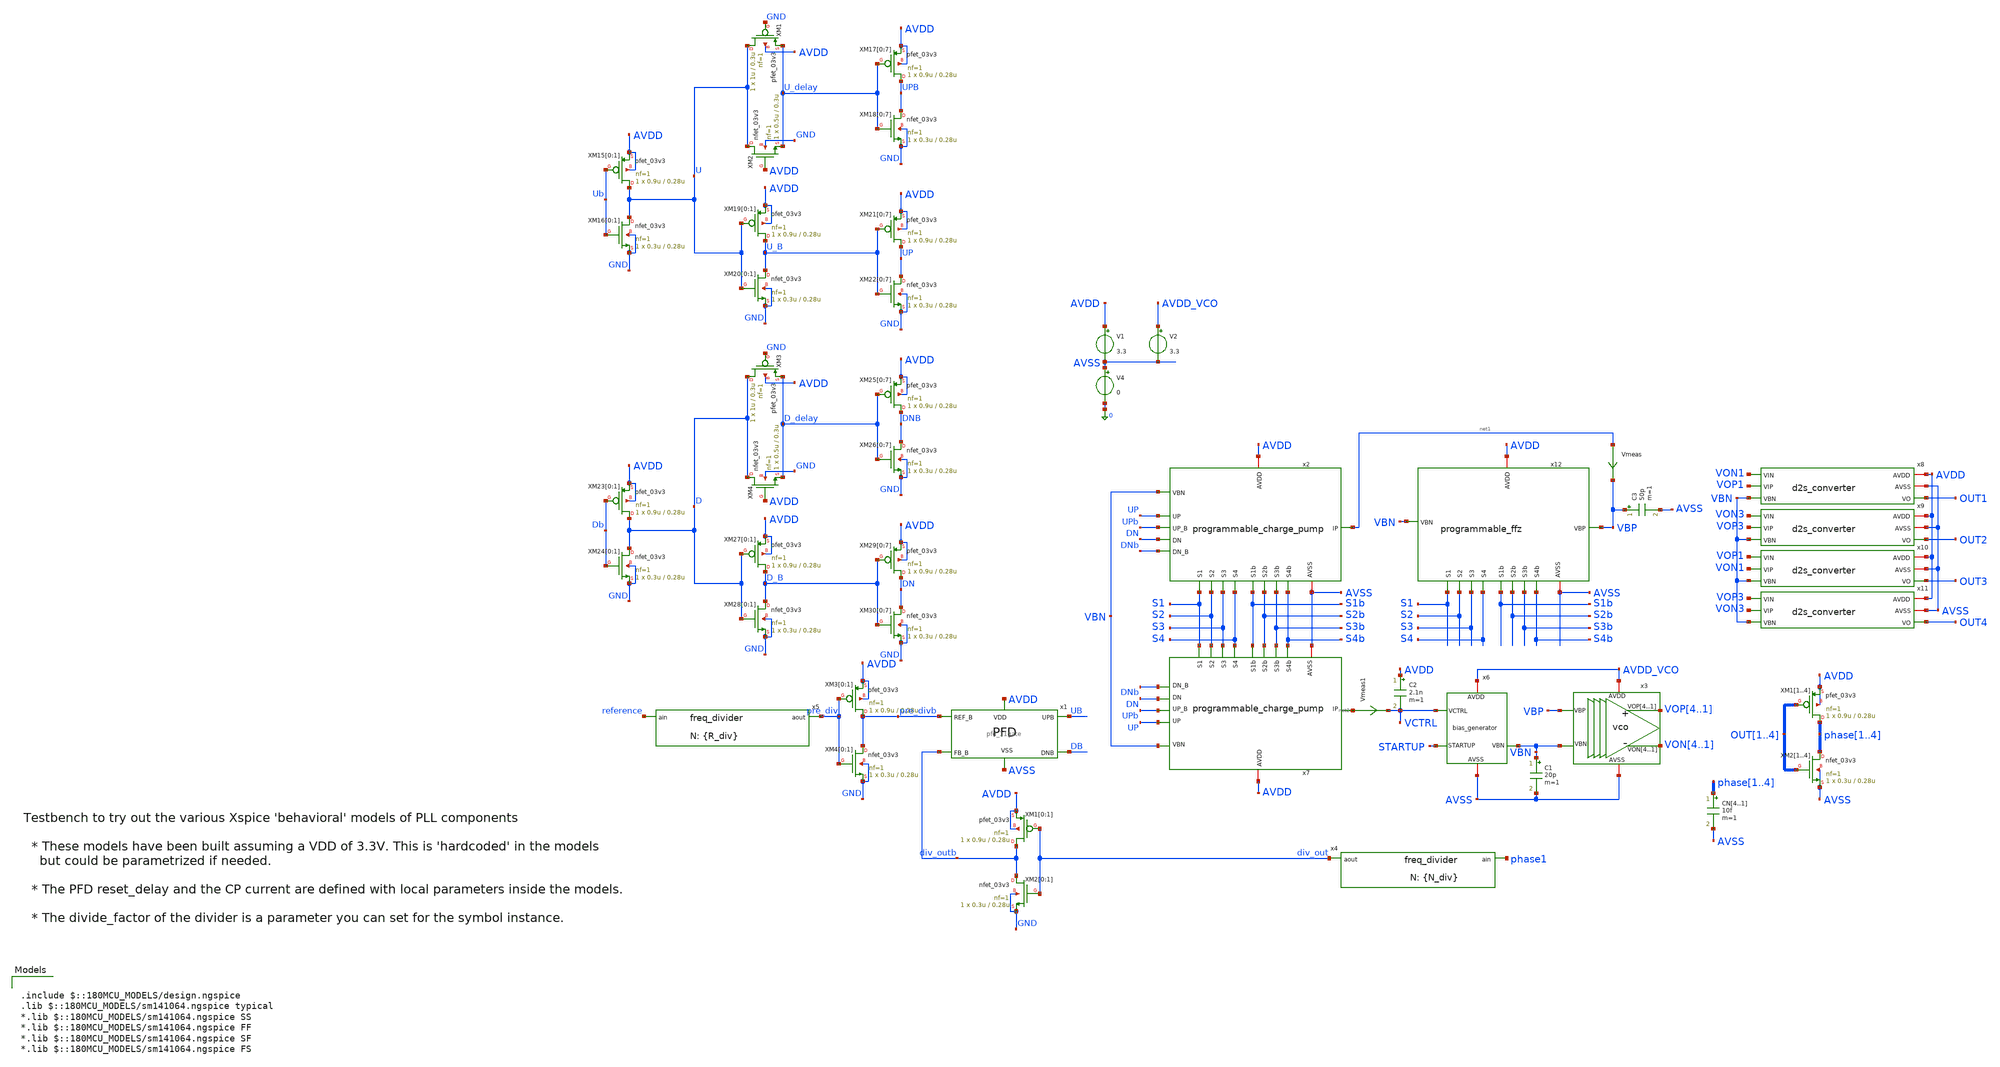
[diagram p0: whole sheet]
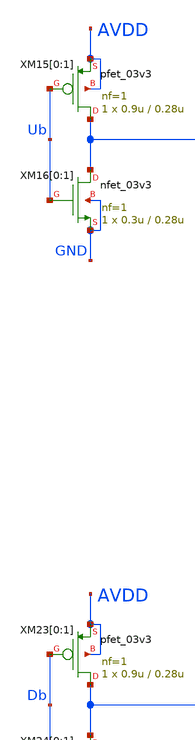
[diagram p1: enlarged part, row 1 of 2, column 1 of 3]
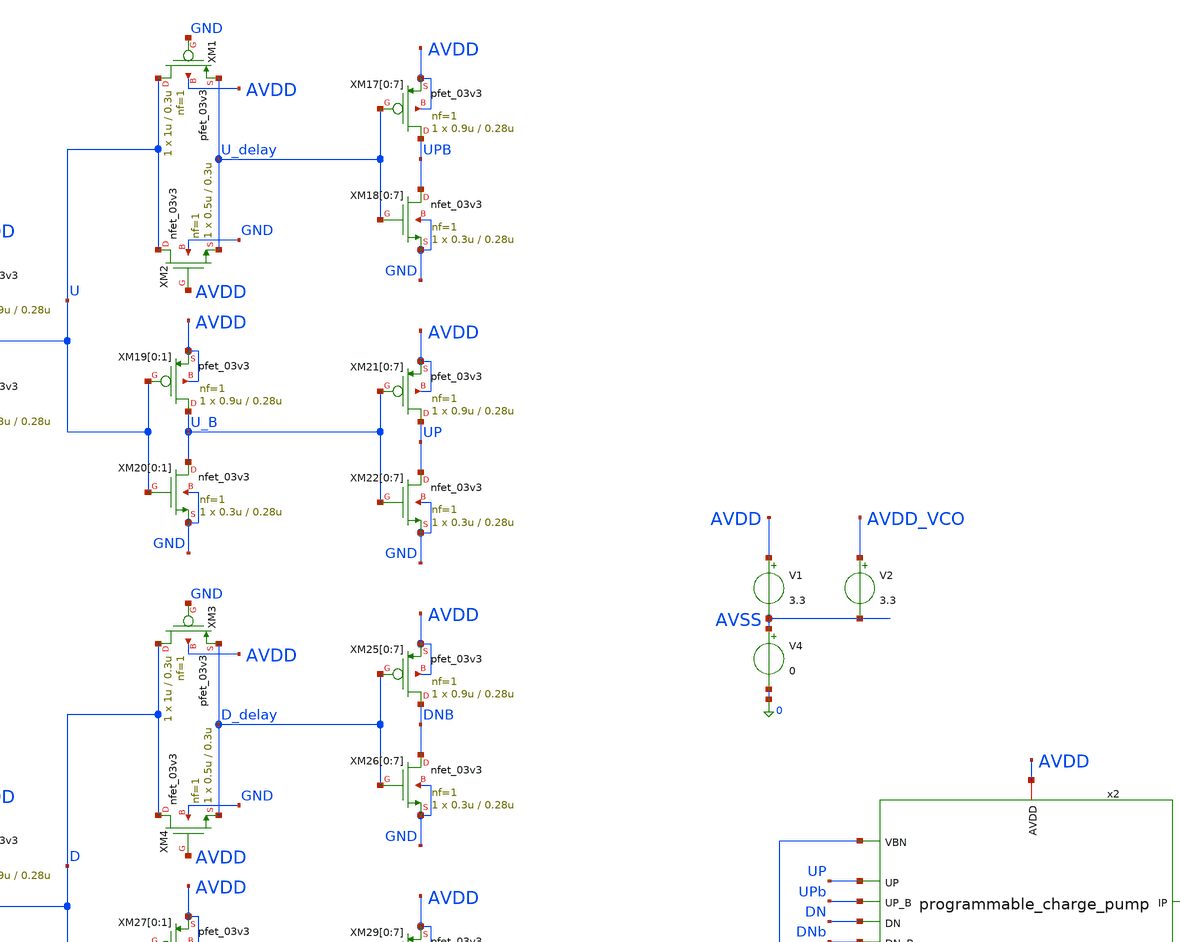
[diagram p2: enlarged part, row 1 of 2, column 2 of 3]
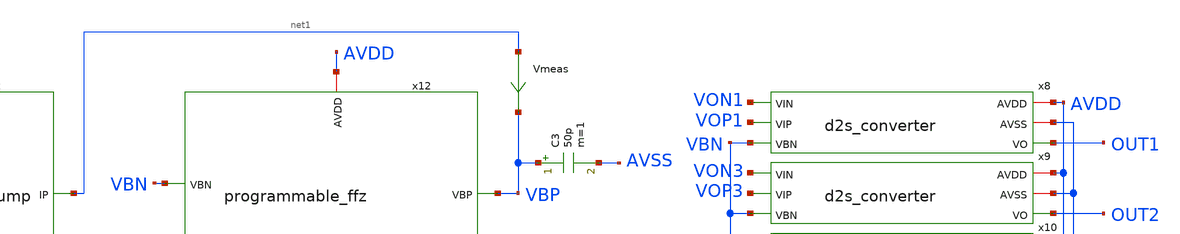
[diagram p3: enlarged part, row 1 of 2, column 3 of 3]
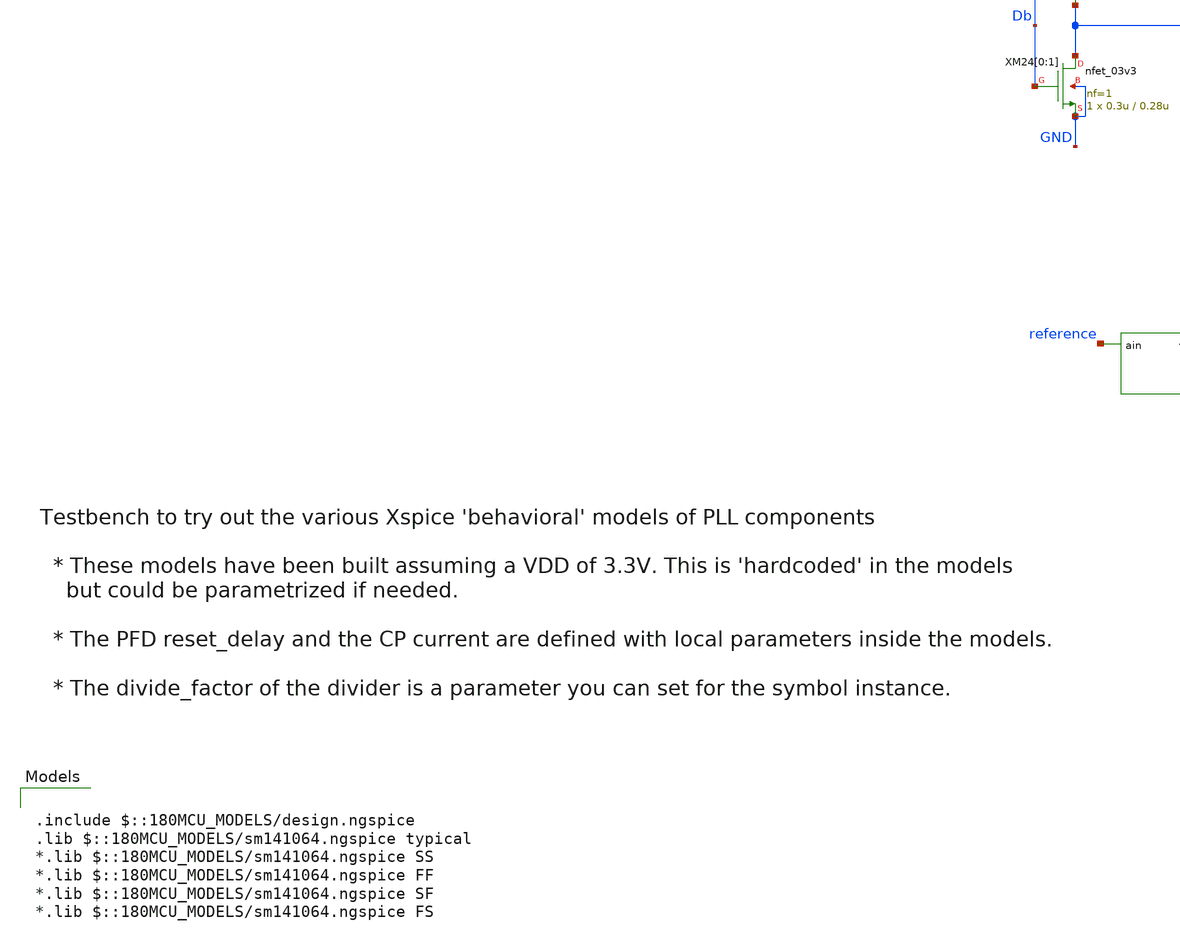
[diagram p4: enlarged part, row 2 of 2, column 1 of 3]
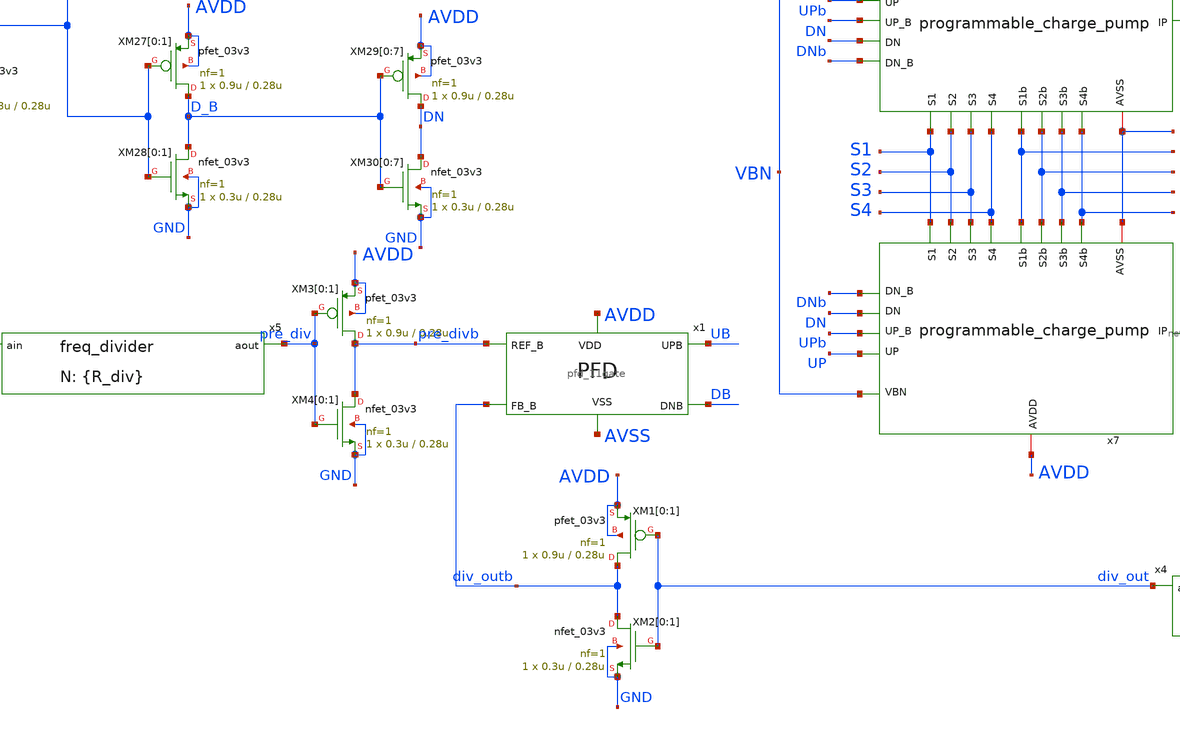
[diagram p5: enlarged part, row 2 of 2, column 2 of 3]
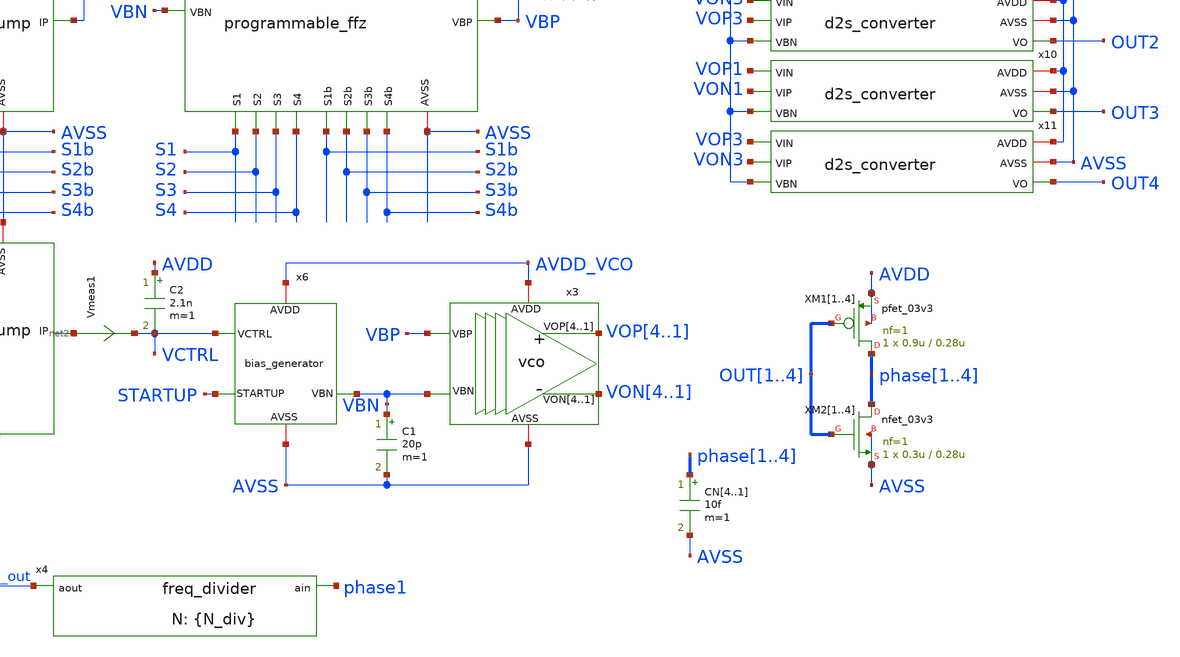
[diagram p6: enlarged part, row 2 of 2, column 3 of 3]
** sch_path: designs/libs/tb_pll/tb_PLL_CP_VCO_PFD_model.sch
**.subckt tb_PLL_CP_VCO_PFD_model
x4 div_out phase1 freq_divider divide_factor={N_div}
x5 pre_div reference freq_divider divide_factor={R_div}
x3 VOP4 VOP3 VOP2 VOP1 VON4 VON3 VON2 VON1 AVDD_VCO AVSS VBP VBN vco
x6 VCTRL AVDD_VCO STARTUP AVSS VBN bias_generator
C2 AVDD VCTRL 2.1n m=1
x8 AVDD AVSS VON1 VOP1 VBN OUT1 d2s_converter
XM11 phase1 OUT1 AVDD AVDD pfet_03v3 L=0.28u W=0.9u nf=1 ad='int((nf+1)/2) * W/nf * 0.18u' as='int((nf+2)/2) * W/nf * 0.18u'
+ pd='2*int((nf+1)/2) * (W/nf + 0.18u)' ps='2*int((nf+2)/2) * (W/nf + 0.18u)' nrd='0.18u / W' nrs='0.18u / W'
+ sa=0 sb=0 sd=0 m=1
XM12 phase2 OUT2 AVDD AVDD pfet_03v3 L=0.28u W=0.9u nf=1 ad='int((nf+1)/2) * W/nf * 0.18u' as='int((nf+2)/2) * W/nf * 0.18u'
+ pd='2*int((nf+1)/2) * (W/nf + 0.18u)' ps='2*int((nf+2)/2) * (W/nf + 0.18u)' nrd='0.18u / W' nrs='0.18u / W'
+ sa=0 sb=0 sd=0 m=1
XM13 phase3 OUT3 AVDD AVDD pfet_03v3 L=0.28u W=0.9u nf=1 ad='int((nf+1)/2) * W/nf * 0.18u' as='int((nf+2)/2) * W/nf * 0.18u'
+ pd='2*int((nf+1)/2) * (W/nf + 0.18u)' ps='2*int((nf+2)/2) * (W/nf + 0.18u)' nrd='0.18u / W' nrs='0.18u / W'
+ sa=0 sb=0 sd=0 m=1
XM14 phase4 OUT4 AVDD AVDD pfet_03v3 L=0.28u W=0.9u nf=1 ad='int((nf+1)/2) * W/nf * 0.18u' as='int((nf+2)/2) * W/nf * 0.18u'
+ pd='2*int((nf+1)/2) * (W/nf + 0.18u)' ps='2*int((nf+2)/2) * (W/nf + 0.18u)' nrd='0.18u / W' nrs='0.18u / W'
+ sa=0 sb=0 sd=0 m=1
XM21 phase1 OUT1 AVSS AVSS nfet_03v3 L=0.28u W=0.3u nf=1 ad='int((nf+1)/2) * W/nf * 0.18u' as='int((nf+2)/2) * W/nf * 0.18u'
+ pd='2*int((nf+1)/2) * (W/nf + 0.18u)' ps='2*int((nf+2)/2) * (W/nf + 0.18u)' nrd='0.18u / W' nrs='0.18u / W'
+ sa=0 sb=0 sd=0 m=1
XM22 phase2 OUT2 AVSS AVSS nfet_03v3 L=0.28u W=0.3u nf=1 ad='int((nf+1)/2) * W/nf * 0.18u' as='int((nf+2)/2) * W/nf * 0.18u'
+ pd='2*int((nf+1)/2) * (W/nf + 0.18u)' ps='2*int((nf+2)/2) * (W/nf + 0.18u)' nrd='0.18u / W' nrs='0.18u / W'
+ sa=0 sb=0 sd=0 m=1
XM23 phase3 OUT3 AVSS AVSS nfet_03v3 L=0.28u W=0.3u nf=1 ad='int((nf+1)/2) * W/nf * 0.18u' as='int((nf+2)/2) * W/nf * 0.18u'
+ pd='2*int((nf+1)/2) * (W/nf + 0.18u)' ps='2*int((nf+2)/2) * (W/nf + 0.18u)' nrd='0.18u / W' nrs='0.18u / W'
+ sa=0 sb=0 sd=0 m=1
XM24 phase4 OUT4 AVSS AVSS nfet_03v3 L=0.28u W=0.3u nf=1 ad='int((nf+1)/2) * W/nf * 0.18u' as='int((nf+2)/2) * W/nf * 0.18u'
+ pd='2*int((nf+1)/2) * (W/nf + 0.18u)' ps='2*int((nf+2)/2) * (W/nf + 0.18u)' nrd='0.18u / W' nrs='0.18u / W'
+ sa=0 sb=0 sd=0 m=1
x9 AVDD AVSS VON3 VOP3 VBN OUT2 d2s_converter
x10 AVDD AVSS VOP1 VON1 VBN OUT3 d2s_converter
x11 AVDD AVSS VOP3 VON3 VBN OUT4 d2s_converter
V1 AVDD AVSS 3.3
V4 AVSS 0 0
V2 AVDD_VCO AVSS 3.3
x2 AVSS AVDD UP UPb DN net1 DNb VBN S1b S1 S2b S2 S3b S3 S4b S4 programmable_charge_pump
x7 AVSS AVDD UP UPb DN net2 DNb VBN S1b S1 S2b S2 S3b S3 S4b S4 programmable_charge_pump
CN4 phase1 AVSS 10f m=1
CN3 phase2 AVSS 10f m=1
CN2 phase3 AVSS 10f m=1
CN1 phase4 AVSS 10f m=1
Vmeas net1 VBP 0
.save i(vmeas)
Vmeas1 net2 VCTRL 0
.save i(vmeas1)
C1 VBN AVSS 20p m=1
C3 VBP AVSS 50p m=1
x12 VBP AVSS AVDD VBN S1b S1 S2b S2 S3b S3 S4b S4 programmable_ffz
x1 pre_divb UB DB div_outb AVDD AVSS pfd_11gate
XM15[0] U Ub AVDD AVDD pfet_03v3 L=0.28u W=0.9u nf=1 ad='int((nf+1)/2) * W/nf * 0.18u' as='int((nf+2)/2) * W/nf * 0.18u'
+ pd='2*int((nf+1)/2) * (W/nf + 0.18u)' ps='2*int((nf+2)/2) * (W/nf + 0.18u)' nrd='0.18u / W' nrs='0.18u / W'
+ sa=0 sb=0 sd=0 m=1
XM15[1] U Ub AVDD AVDD pfet_03v3 L=0.28u W=0.9u nf=1 ad='int((nf+1)/2) * W/nf * 0.18u' as='int((nf+2)/2) * W/nf * 0.18u'
+ pd='2*int((nf+1)/2) * (W/nf + 0.18u)' ps='2*int((nf+2)/2) * (W/nf + 0.18u)' nrd='0.18u / W' nrs='0.18u / W'
+ sa=0 sb=0 sd=0 m=1
XM16[0] U Ub GND GND nfet_03v3 L=0.28u W=0.3u nf=1 ad='int((nf+1)/2) * W/nf * 0.18u' as='int((nf+2)/2) * W/nf * 0.18u'
+ pd='2*int((nf+1)/2) * (W/nf + 0.18u)' ps='2*int((nf+2)/2) * (W/nf + 0.18u)' nrd='0.18u / W' nrs='0.18u / W'
+ sa=0 sb=0 sd=0 m=1
XM16[1] U Ub GND GND nfet_03v3 L=0.28u W=0.3u nf=1 ad='int((nf+1)/2) * W/nf * 0.18u' as='int((nf+2)/2) * W/nf * 0.18u'
+ pd='2*int((nf+1)/2) * (W/nf + 0.18u)' ps='2*int((nf+2)/2) * (W/nf + 0.18u)' nrd='0.18u / W' nrs='0.18u / W'
+ sa=0 sb=0 sd=0 m=1
XM1 U GND U_delay AVDD pfet_03v3 L=0.3u W=1u nf=1 ad='int((nf+1)/2) * W/nf * 0.18u' as='int((nf+2)/2) * W/nf * 0.18u'
+ pd='2*int((nf+1)/2) * (W/nf + 0.18u)' ps='2*int((nf+2)/2) * (W/nf + 0.18u)' nrd='0.18u / W' nrs='0.18u / W'
+ sa=0 sb=0 sd=0 m=1
XM2 U AVDD U_delay GND nfet_03v3 L=0.3u W=0.5u nf=1 ad='int((nf+1)/2) * W/nf * 0.18u' as='int((nf+2)/2) * W/nf * 0.18u'
+ pd='2*int((nf+1)/2) * (W/nf + 0.18u)' ps='2*int((nf+2)/2) * (W/nf + 0.18u)' nrd='0.18u / W' nrs='0.18u / W'
+ sa=0 sb=0 sd=0 m=1
XM17[0] UPB U_delay AVDD AVDD pfet_03v3 L=0.28u W=0.9u nf=1 ad='int((nf+1)/2) * W/nf * 0.18u' as='int((nf+2)/2) * W/nf * 0.18u'
+ pd='2*int((nf+1)/2) * (W/nf + 0.18u)' ps='2*int((nf+2)/2) * (W/nf + 0.18u)' nrd='0.18u / W' nrs='0.18u / W'
+ sa=0 sb=0 sd=0 m=1
XM17[1] UPB U_delay AVDD AVDD pfet_03v3 L=0.28u W=0.9u nf=1 ad='int((nf+1)/2) * W/nf * 0.18u' as='int((nf+2)/2) * W/nf * 0.18u'
+ pd='2*int((nf+1)/2) * (W/nf + 0.18u)' ps='2*int((nf+2)/2) * (W/nf + 0.18u)' nrd='0.18u / W' nrs='0.18u / W'
+ sa=0 sb=0 sd=0 m=1
XM17[2] UPB U_delay AVDD AVDD pfet_03v3 L=0.28u W=0.9u nf=1 ad='int((nf+1)/2) * W/nf * 0.18u' as='int((nf+2)/2) * W/nf * 0.18u'
+ pd='2*int((nf+1)/2) * (W/nf + 0.18u)' ps='2*int((nf+2)/2) * (W/nf + 0.18u)' nrd='0.18u / W' nrs='0.18u / W'
+ sa=0 sb=0 sd=0 m=1
XM17[3] UPB U_delay AVDD AVDD pfet_03v3 L=0.28u W=0.9u nf=1 ad='int((nf+1)/2) * W/nf * 0.18u' as='int((nf+2)/2) * W/nf * 0.18u'
+ pd='2*int((nf+1)/2) * (W/nf + 0.18u)' ps='2*int((nf+2)/2) * (W/nf + 0.18u)' nrd='0.18u / W' nrs='0.18u / W'
+ sa=0 sb=0 sd=0 m=1
XM17[4] UPB U_delay AVDD AVDD pfet_03v3 L=0.28u W=0.9u nf=1 ad='int((nf+1)/2) * W/nf * 0.18u' as='int((nf+2)/2) * W/nf * 0.18u'
+ pd='2*int((nf+1)/2) * (W/nf + 0.18u)' ps='2*int((nf+2)/2) * (W/nf + 0.18u)' nrd='0.18u / W' nrs='0.18u / W'
+ sa=0 sb=0 sd=0 m=1
XM17[5] UPB U_delay AVDD AVDD pfet_03v3 L=0.28u W=0.9u nf=1 ad='int((nf+1)/2) * W/nf * 0.18u' as='int((nf+2)/2) * W/nf * 0.18u'
+ pd='2*int((nf+1)/2) * (W/nf + 0.18u)' ps='2*int((nf+2)/2) * (W/nf + 0.18u)' nrd='0.18u / W' nrs='0.18u / W'
+ sa=0 sb=0 sd=0 m=1
XM17[6] UPB U_delay AVDD AVDD pfet_03v3 L=0.28u W=0.9u nf=1 ad='int((nf+1)/2) * W/nf * 0.18u' as='int((nf+2)/2) * W/nf * 0.18u'
+ pd='2*int((nf+1)/2) * (W/nf + 0.18u)' ps='2*int((nf+2)/2) * (W/nf + 0.18u)' nrd='0.18u / W' nrs='0.18u / W'
+ sa=0 sb=0 sd=0 m=1
XM17[7] UPB U_delay AVDD AVDD pfet_03v3 L=0.28u W=0.9u nf=1 ad='int((nf+1)/2) * W/nf * 0.18u' as='int((nf+2)/2) * W/nf * 0.18u'
+ pd='2*int((nf+1)/2) * (W/nf + 0.18u)' ps='2*int((nf+2)/2) * (W/nf + 0.18u)' nrd='0.18u / W' nrs='0.18u / W'
+ sa=0 sb=0 sd=0 m=1
XM18[0] UPB U_delay GND GND nfet_03v3 L=0.28u W=0.3u nf=1 ad='int((nf+1)/2) * W/nf * 0.18u' as='int((nf+2)/2) * W/nf * 0.18u'
+ pd='2*int((nf+1)/2) * (W/nf + 0.18u)' ps='2*int((nf+2)/2) * (W/nf + 0.18u)' nrd='0.18u / W' nrs='0.18u / W'
+ sa=0 sb=0 sd=0 m=1
XM18[1] UPB U_delay GND GND nfet_03v3 L=0.28u W=0.3u nf=1 ad='int((nf+1)/2) * W/nf * 0.18u' as='int((nf+2)/2) * W/nf * 0.18u'
+ pd='2*int((nf+1)/2) * (W/nf + 0.18u)' ps='2*int((nf+2)/2) * (W/nf + 0.18u)' nrd='0.18u / W' nrs='0.18u / W'
+ sa=0 sb=0 sd=0 m=1
XM18[2] UPB U_delay GND GND nfet_03v3 L=0.28u W=0.3u nf=1 ad='int((nf+1)/2) * W/nf * 0.18u' as='int((nf+2)/2) * W/nf * 0.18u'
+ pd='2*int((nf+1)/2) * (W/nf + 0.18u)' ps='2*int((nf+2)/2) * (W/nf + 0.18u)' nrd='0.18u / W' nrs='0.18u / W'
+ sa=0 sb=0 sd=0 m=1
XM18[3] UPB U_delay GND GND nfet_03v3 L=0.28u W=0.3u nf=1 ad='int((nf+1)/2) * W/nf * 0.18u' as='int((nf+2)/2) * W/nf * 0.18u'
+ pd='2*int((nf+1)/2) * (W/nf + 0.18u)' ps='2*int((nf+2)/2) * (W/nf + 0.18u)' nrd='0.18u / W' nrs='0.18u / W'
+ sa=0 sb=0 sd=0 m=1
XM18[4] UPB U_delay GND GND nfet_03v3 L=0.28u W=0.3u nf=1 ad='int((nf+1)/2) * W/nf * 0.18u' as='int((nf+2)/2) * W/nf * 0.18u'
+ pd='2*int((nf+1)/2) * (W/nf + 0.18u)' ps='2*int((nf+2)/2) * (W/nf + 0.18u)' nrd='0.18u / W' nrs='0.18u / W'
+ sa=0 sb=0 sd=0 m=1
XM18[5] UPB U_delay GND GND nfet_03v3 L=0.28u W=0.3u nf=1 ad='int((nf+1)/2) * W/nf * 0.18u' as='int((nf+2)/2) * W/nf * 0.18u'
+ pd='2*int((nf+1)/2) * (W/nf + 0.18u)' ps='2*int((nf+2)/2) * (W/nf + 0.18u)' nrd='0.18u / W' nrs='0.18u / W'
+ sa=0 sb=0 sd=0 m=1
XM18[6] UPB U_delay GND GND nfet_03v3 L=0.28u W=0.3u nf=1 ad='int((nf+1)/2) * W/nf * 0.18u' as='int((nf+2)/2) * W/nf * 0.18u'
+ pd='2*int((nf+1)/2) * (W/nf + 0.18u)' ps='2*int((nf+2)/2) * (W/nf + 0.18u)' nrd='0.18u / W' nrs='0.18u / W'
+ sa=0 sb=0 sd=0 m=1
XM18[7] UPB U_delay GND GND nfet_03v3 L=0.28u W=0.3u nf=1 ad='int((nf+1)/2) * W/nf * 0.18u' as='int((nf+2)/2) * W/nf * 0.18u'
+ pd='2*int((nf+1)/2) * (W/nf + 0.18u)' ps='2*int((nf+2)/2) * (W/nf + 0.18u)' nrd='0.18u / W' nrs='0.18u / W'
+ sa=0 sb=0 sd=0 m=1
XM19[0] U_B U AVDD AVDD pfet_03v3 L=0.28u W=0.9u nf=1 ad='int((nf+1)/2) * W/nf * 0.18u' as='int((nf+2)/2) * W/nf * 0.18u'
+ pd='2*int((nf+1)/2) * (W/nf + 0.18u)' ps='2*int((nf+2)/2) * (W/nf + 0.18u)' nrd='0.18u / W' nrs='0.18u / W'
+ sa=0 sb=0 sd=0 m=1
XM19[1] U_B U AVDD AVDD pfet_03v3 L=0.28u W=0.9u nf=1 ad='int((nf+1)/2) * W/nf * 0.18u' as='int((nf+2)/2) * W/nf * 0.18u'
+ pd='2*int((nf+1)/2) * (W/nf + 0.18u)' ps='2*int((nf+2)/2) * (W/nf + 0.18u)' nrd='0.18u / W' nrs='0.18u / W'
+ sa=0 sb=0 sd=0 m=1
XM20[0] U_B U GND GND nfet_03v3 L=0.28u W=0.3u nf=1 ad='int((nf+1)/2) * W/nf * 0.18u' as='int((nf+2)/2) * W/nf * 0.18u'
+ pd='2*int((nf+1)/2) * (W/nf + 0.18u)' ps='2*int((nf+2)/2) * (W/nf + 0.18u)' nrd='0.18u / W' nrs='0.18u / W'
+ sa=0 sb=0 sd=0 m=1
XM20[1] U_B U GND GND nfet_03v3 L=0.28u W=0.3u nf=1 ad='int((nf+1)/2) * W/nf * 0.18u' as='int((nf+2)/2) * W/nf * 0.18u'
+ pd='2*int((nf+1)/2) * (W/nf + 0.18u)' ps='2*int((nf+2)/2) * (W/nf + 0.18u)' nrd='0.18u / W' nrs='0.18u / W'
+ sa=0 sb=0 sd=0 m=1
XM21[0] UP U_B AVDD AVDD pfet_03v3 L=0.28u W=0.9u nf=1 ad='int((nf+1)/2) * W/nf * 0.18u' as='int((nf+2)/2) * W/nf * 0.18u'
+ pd='2*int((nf+1)/2) * (W/nf + 0.18u)' ps='2*int((nf+2)/2) * (W/nf + 0.18u)' nrd='0.18u / W' nrs='0.18u / W'
+ sa=0 sb=0 sd=0 m=1
XM21[1] UP U_B AVDD AVDD pfet_03v3 L=0.28u W=0.9u nf=1 ad='int((nf+1)/2) * W/nf * 0.18u' as='int((nf+2)/2) * W/nf * 0.18u'
+ pd='2*int((nf+1)/2) * (W/nf + 0.18u)' ps='2*int((nf+2)/2) * (W/nf + 0.18u)' nrd='0.18u / W' nrs='0.18u / W'
+ sa=0 sb=0 sd=0 m=1
XM21[2] UP U_B AVDD AVDD pfet_03v3 L=0.28u W=0.9u nf=1 ad='int((nf+1)/2) * W/nf * 0.18u' as='int((nf+2)/2) * W/nf * 0.18u'
+ pd='2*int((nf+1)/2) * (W/nf + 0.18u)' ps='2*int((nf+2)/2) * (W/nf + 0.18u)' nrd='0.18u / W' nrs='0.18u / W'
+ sa=0 sb=0 sd=0 m=1
XM21[3] UP U_B AVDD AVDD pfet_03v3 L=0.28u W=0.9u nf=1 ad='int((nf+1)/2) * W/nf * 0.18u' as='int((nf+2)/2) * W/nf * 0.18u'
+ pd='2*int((nf+1)/2) * (W/nf + 0.18u)' ps='2*int((nf+2)/2) * (W/nf + 0.18u)' nrd='0.18u / W' nrs='0.18u / W'
+ sa=0 sb=0 sd=0 m=1
XM21[4] UP U_B AVDD AVDD pfet_03v3 L=0.28u W=0.9u nf=1 ad='int((nf+1)/2) * W/nf * 0.18u' as='int((nf+2)/2) * W/nf * 0.18u'
+ pd='2*int((nf+1)/2) * (W/nf + 0.18u)' ps='2*int((nf+2)/2) * (W/nf + 0.18u)' nrd='0.18u / W' nrs='0.18u / W'
+ sa=0 sb=0 sd=0 m=1
XM21[5] UP U_B AVDD AVDD pfet_03v3 L=0.28u W=0.9u nf=1 ad='int((nf+1)/2) * W/nf * 0.18u' as='int((nf+2)/2) * W/nf * 0.18u'
+ pd='2*int((nf+1)/2) * (W/nf + 0.18u)' ps='2*int((nf+2)/2) * (W/nf + 0.18u)' nrd='0.18u / W' nrs='0.18u / W'
+ sa=0 sb=0 sd=0 m=1
XM21[6] UP U_B AVDD AVDD pfet_03v3 L=0.28u W=0.9u nf=1 ad='int((nf+1)/2) * W/nf * 0.18u' as='int((nf+2)/2) * W/nf * 0.18u'
+ pd='2*int((nf+1)/2) * (W/nf + 0.18u)' ps='2*int((nf+2)/2) * (W/nf + 0.18u)' nrd='0.18u / W' nrs='0.18u / W'
+ sa=0 sb=0 sd=0 m=1
XM21[7] UP U_B AVDD AVDD pfet_03v3 L=0.28u W=0.9u nf=1 ad='int((nf+1)/2) * W/nf * 0.18u' as='int((nf+2)/2) * W/nf * 0.18u'
+ pd='2*int((nf+1)/2) * (W/nf + 0.18u)' ps='2*int((nf+2)/2) * (W/nf + 0.18u)' nrd='0.18u / W' nrs='0.18u / W'
+ sa=0 sb=0 sd=0 m=1
XM22[0] UP U_B GND GND nfet_03v3 L=0.28u W=0.3u nf=1 ad='int((nf+1)/2) * W/nf * 0.18u' as='int((nf+2)/2) * W/nf * 0.18u'
+ pd='2*int((nf+1)/2) * (W/nf + 0.18u)' ps='2*int((nf+2)/2) * (W/nf + 0.18u)' nrd='0.18u / W' nrs='0.18u / W'
+ sa=0 sb=0 sd=0 m=1
XM22[1] UP U_B GND GND nfet_03v3 L=0.28u W=0.3u nf=1 ad='int((nf+1)/2) * W/nf * 0.18u' as='int((nf+2)/2) * W/nf * 0.18u'
+ pd='2*int((nf+1)/2) * (W/nf + 0.18u)' ps='2*int((nf+2)/2) * (W/nf + 0.18u)' nrd='0.18u / W' nrs='0.18u / W'
+ sa=0 sb=0 sd=0 m=1
XM22[2] UP U_B GND GND nfet_03v3 L=0.28u W=0.3u nf=1 ad='int((nf+1)/2) * W/nf * 0.18u' as='int((nf+2)/2) * W/nf * 0.18u'
+ pd='2*int((nf+1)/2) * (W/nf + 0.18u)' ps='2*int((nf+2)/2) * (W/nf + 0.18u)' nrd='0.18u / W' nrs='0.18u / W'
+ sa=0 sb=0 sd=0 m=1
XM22[3] UP U_B GND GND nfet_03v3 L=0.28u W=0.3u nf=1 ad='int((nf+1)/2) * W/nf * 0.18u' as='int((nf+2)/2) * W/nf * 0.18u'
+ pd='2*int((nf+1)/2) * (W/nf + 0.18u)' ps='2*int((nf+2)/2) * (W/nf + 0.18u)' nrd='0.18u / W' nrs='0.18u / W'
+ sa=0 sb=0 sd=0 m=1
XM22[4] UP U_B GND GND nfet_03v3 L=0.28u W=0.3u nf=1 ad='int((nf+1)/2) * W/nf * 0.18u' as='int((nf+2)/2) * W/nf * 0.18u'
+ pd='2*int((nf+1)/2) * (W/nf + 0.18u)' ps='2*int((nf+2)/2) * (W/nf + 0.18u)' nrd='0.18u / W' nrs='0.18u / W'
+ sa=0 sb=0 sd=0 m=1
XM22[5] UP U_B GND GND nfet_03v3 L=0.28u W=0.3u nf=1 ad='int((nf+1)/2) * W/nf * 0.18u' as='int((nf+2)/2) * W/nf * 0.18u'
+ pd='2*int((nf+1)/2) * (W/nf + 0.18u)' ps='2*int((nf+2)/2) * (W/nf + 0.18u)' nrd='0.18u / W' nrs='0.18u / W'
+ sa=0 sb=0 sd=0 m=1
XM22[6] UP U_B GND GND nfet_03v3 L=0.28u W=0.3u nf=1 ad='int((nf+1)/2) * W/nf * 0.18u' as='int((nf+2)/2) * W/nf * 0.18u'
+ pd='2*int((nf+1)/2) * (W/nf + 0.18u)' ps='2*int((nf+2)/2) * (W/nf + 0.18u)' nrd='0.18u / W' nrs='0.18u / W'
+ sa=0 sb=0 sd=0 m=1
XM22[7] UP U_B GND GND nfet_03v3 L=0.28u W=0.3u nf=1 ad='int((nf+1)/2) * W/nf * 0.18u' as='int((nf+2)/2) * W/nf * 0.18u'
+ pd='2*int((nf+1)/2) * (W/nf + 0.18u)' ps='2*int((nf+2)/2) * (W/nf + 0.18u)' nrd='0.18u / W' nrs='0.18u / W'
+ sa=0 sb=0 sd=0 m=1
XM23[0] D Db AVDD AVDD pfet_03v3 L=0.28u W=0.9u nf=1 ad='int((nf+1)/2) * W/nf * 0.18u' as='int((nf+2)/2) * W/nf * 0.18u'
+ pd='2*int((nf+1)/2) * (W/nf + 0.18u)' ps='2*int((nf+2)/2) * (W/nf + 0.18u)' nrd='0.18u / W' nrs='0.18u / W'
+ sa=0 sb=0 sd=0 m=1
XM23[1] D Db AVDD AVDD pfet_03v3 L=0.28u W=0.9u nf=1 ad='int((nf+1)/2) * W/nf * 0.18u' as='int((nf+2)/2) * W/nf * 0.18u'
+ pd='2*int((nf+1)/2) * (W/nf + 0.18u)' ps='2*int((nf+2)/2) * (W/nf + 0.18u)' nrd='0.18u / W' nrs='0.18u / W'
+ sa=0 sb=0 sd=0 m=1
XM24[0] D Db GND GND nfet_03v3 L=0.28u W=0.3u nf=1 ad='int((nf+1)/2) * W/nf * 0.18u' as='int((nf+2)/2) * W/nf * 0.18u'
+ pd='2*int((nf+1)/2) * (W/nf + 0.18u)' ps='2*int((nf+2)/2) * (W/nf + 0.18u)' nrd='0.18u / W' nrs='0.18u / W'
+ sa=0 sb=0 sd=0 m=1
XM24[1] D Db GND GND nfet_03v3 L=0.28u W=0.3u nf=1 ad='int((nf+1)/2) * W/nf * 0.18u' as='int((nf+2)/2) * W/nf * 0.18u'
+ pd='2*int((nf+1)/2) * (W/nf + 0.18u)' ps='2*int((nf+2)/2) * (W/nf + 0.18u)' nrd='0.18u / W' nrs='0.18u / W'
+ sa=0 sb=0 sd=0 m=1
XM25[0] DNB D_delay AVDD AVDD pfet_03v3 L=0.28u W=0.9u nf=1 ad='int((nf+1)/2) * W/nf * 0.18u' as='int((nf+2)/2) * W/nf * 0.18u'
+ pd='2*int((nf+1)/2) * (W/nf + 0.18u)' ps='2*int((nf+2)/2) * (W/nf + 0.18u)' nrd='0.18u / W' nrs='0.18u / W'
+ sa=0 sb=0 sd=0 m=1
XM25[1] DNB D_delay AVDD AVDD pfet_03v3 L=0.28u W=0.9u nf=1 ad='int((nf+1)/2) * W/nf * 0.18u' as='int((nf+2)/2) * W/nf * 0.18u'
+ pd='2*int((nf+1)/2) * (W/nf + 0.18u)' ps='2*int((nf+2)/2) * (W/nf + 0.18u)' nrd='0.18u / W' nrs='0.18u / W'
+ sa=0 sb=0 sd=0 m=1
XM25[2] DNB D_delay AVDD AVDD pfet_03v3 L=0.28u W=0.9u nf=1 ad='int((nf+1)/2) * W/nf * 0.18u' as='int((nf+2)/2) * W/nf * 0.18u'
+ pd='2*int((nf+1)/2) * (W/nf + 0.18u)' ps='2*int((nf+2)/2) * (W/nf + 0.18u)' nrd='0.18u / W' nrs='0.18u / W'
+ sa=0 sb=0 sd=0 m=1
XM25[3] DNB D_delay AVDD AVDD pfet_03v3 L=0.28u W=0.9u nf=1 ad='int((nf+1)/2) * W/nf * 0.18u' as='int((nf+2)/2) * W/nf * 0.18u'
+ pd='2*int((nf+1)/2) * (W/nf + 0.18u)' ps='2*int((nf+2)/2) * (W/nf + 0.18u)' nrd='0.18u / W' nrs='0.18u / W'
+ sa=0 sb=0 sd=0 m=1
XM25[4] DNB D_delay AVDD AVDD pfet_03v3 L=0.28u W=0.9u nf=1 ad='int((nf+1)/2) * W/nf * 0.18u' as='int((nf+2)/2) * W/nf * 0.18u'
+ pd='2*int((nf+1)/2) * (W/nf + 0.18u)' ps='2*int((nf+2)/2) * (W/nf + 0.18u)' nrd='0.18u / W' nrs='0.18u / W'
+ sa=0 sb=0 sd=0 m=1
XM25[5] DNB D_delay AVDD AVDD pfet_03v3 L=0.28u W=0.9u nf=1 ad='int((nf+1)/2) * W/nf * 0.18u' as='int((nf+2)/2) * W/nf * 0.18u'
+ pd='2*int((nf+1)/2) * (W/nf + 0.18u)' ps='2*int((nf+2)/2) * (W/nf + 0.18u)' nrd='0.18u / W' nrs='0.18u / W'
+ sa=0 sb=0 sd=0 m=1
XM25[6] DNB D_delay AVDD AVDD pfet_03v3 L=0.28u W=0.9u nf=1 ad='int((nf+1)/2) * W/nf * 0.18u' as='int((nf+2)/2) * W/nf * 0.18u'
+ pd='2*int((nf+1)/2) * (W/nf + 0.18u)' ps='2*int((nf+2)/2) * (W/nf + 0.18u)' nrd='0.18u / W' nrs='0.18u / W'
+ sa=0 sb=0 sd=0 m=1
XM25[7] DNB D_delay AVDD AVDD pfet_03v3 L=0.28u W=0.9u nf=1 ad='int((nf+1)/2) * W/nf * 0.18u' as='int((nf+2)/2) * W/nf * 0.18u'
+ pd='2*int((nf+1)/2) * (W/nf + 0.18u)' ps='2*int((nf+2)/2) * (W/nf + 0.18u)' nrd='0.18u / W' nrs='0.18u / W'
+ sa=0 sb=0 sd=0 m=1
XM26[0] DNB D_delay GND GND nfet_03v3 L=0.28u W=0.3u nf=1 ad='int((nf+1)/2) * W/nf * 0.18u' as='int((nf+2)/2) * W/nf * 0.18u'
+ pd='2*int((nf+1)/2) * (W/nf + 0.18u)' ps='2*int((nf+2)/2) * (W/nf + 0.18u)' nrd='0.18u / W' nrs='0.18u / W'
+ sa=0 sb=0 sd=0 m=1
XM26[1] DNB D_delay GND GND nfet_03v3 L=0.28u W=0.3u nf=1 ad='int((nf+1)/2) * W/nf * 0.18u' as='int((nf+2)/2) * W/nf * 0.18u'
+ pd='2*int((nf+1)/2) * (W/nf + 0.18u)' ps='2*int((nf+2)/2) * (W/nf + 0.18u)' nrd='0.18u / W' nrs='0.18u / W'
+ sa=0 sb=0 sd=0 m=1
XM26[2] DNB D_delay GND GND nfet_03v3 L=0.28u W=0.3u nf=1 ad='int((nf+1)/2) * W/nf * 0.18u' as='int((nf+2)/2) * W/nf * 0.18u'
+ pd='2*int((nf+1)/2) * (W/nf + 0.18u)' ps='2*int((nf+2)/2) * (W/nf + 0.18u)' nrd='0.18u / W' nrs='0.18u / W'
+ sa=0 sb=0 sd=0 m=1
XM26[3] DNB D_delay GND GND nfet_03v3 L=0.28u W=0.3u nf=1 ad='int((nf+1)/2) * W/nf * 0.18u' as='int((nf+2)/2) * W/nf * 0.18u'
+ pd='2*int((nf+1)/2) * (W/nf + 0.18u)' ps='2*int((nf+2)/2) * (W/nf + 0.18u)' nrd='0.18u / W' nrs='0.18u / W'
+ sa=0 sb=0 sd=0 m=1
XM26[4] DNB D_delay GND GND nfet_03v3 L=0.28u W=0.3u nf=1 ad='int((nf+1)/2) * W/nf * 0.18u' as='int((nf+2)/2) * W/nf * 0.18u'
+ pd='2*int((nf+1)/2) * (W/nf + 0.18u)' ps='2*int((nf+2)/2) * (W/nf + 0.18u)' nrd='0.18u / W' nrs='0.18u / W'
+ sa=0 sb=0 sd=0 m=1
XM26[5] DNB D_delay GND GND nfet_03v3 L=0.28u W=0.3u nf=1 ad='int((nf+1)/2) * W/nf * 0.18u' as='int((nf+2)/2) * W/nf * 0.18u'
+ pd='2*int((nf+1)/2) * (W/nf + 0.18u)' ps='2*int((nf+2)/2) * (W/nf + 0.18u)' nrd='0.18u / W' nrs='0.18u / W'
+ sa=0 sb=0 sd=0 m=1
XM26[6] DNB D_delay GND GND nfet_03v3 L=0.28u W=0.3u nf=1 ad='int((nf+1)/2) * W/nf * 0.18u' as='int((nf+2)/2) * W/nf * 0.18u'
+ pd='2*int((nf+1)/2) * (W/nf + 0.18u)' ps='2*int((nf+2)/2) * (W/nf + 0.18u)' nrd='0.18u / W' nrs='0.18u / W'
+ sa=0 sb=0 sd=0 m=1
XM26[7] DNB D_delay GND GND nfet_03v3 L=0.28u W=0.3u nf=1 ad='int((nf+1)/2) * W/nf * 0.18u' as='int((nf+2)/2) * W/nf * 0.18u'
+ pd='2*int((nf+1)/2) * (W/nf + 0.18u)' ps='2*int((nf+2)/2) * (W/nf + 0.18u)' nrd='0.18u / W' nrs='0.18u / W'
+ sa=0 sb=0 sd=0 m=1
XM27[0] D_B D AVDD AVDD pfet_03v3 L=0.28u W=0.9u nf=1 ad='int((nf+1)/2) * W/nf * 0.18u' as='int((nf+2)/2) * W/nf * 0.18u'
+ pd='2*int((nf+1)/2) * (W/nf + 0.18u)' ps='2*int((nf+2)/2) * (W/nf + 0.18u)' nrd='0.18u / W' nrs='0.18u / W'
+ sa=0 sb=0 sd=0 m=1
XM27[1] D_B D AVDD AVDD pfet_03v3 L=0.28u W=0.9u nf=1 ad='int((nf+1)/2) * W/nf * 0.18u' as='int((nf+2)/2) * W/nf * 0.18u'
+ pd='2*int((nf+1)/2) * (W/nf + 0.18u)' ps='2*int((nf+2)/2) * (W/nf + 0.18u)' nrd='0.18u / W' nrs='0.18u / W'
+ sa=0 sb=0 sd=0 m=1
XM28[0] D_B D GND GND nfet_03v3 L=0.28u W=0.3u nf=1 ad='int((nf+1)/2) * W/nf * 0.18u' as='int((nf+2)/2) * W/nf * 0.18u'
+ pd='2*int((nf+1)/2) * (W/nf + 0.18u)' ps='2*int((nf+2)/2) * (W/nf + 0.18u)' nrd='0.18u / W' nrs='0.18u / W'
+ sa=0 sb=0 sd=0 m=1
XM28[1] D_B D GND GND nfet_03v3 L=0.28u W=0.3u nf=1 ad='int((nf+1)/2) * W/nf * 0.18u' as='int((nf+2)/2) * W/nf * 0.18u'
+ pd='2*int((nf+1)/2) * (W/nf + 0.18u)' ps='2*int((nf+2)/2) * (W/nf + 0.18u)' nrd='0.18u / W' nrs='0.18u / W'
+ sa=0 sb=0 sd=0 m=1
XM29[0] DN D_B AVDD AVDD pfet_03v3 L=0.28u W=0.9u nf=1 ad='int((nf+1)/2) * W/nf * 0.18u' as='int((nf+2)/2) * W/nf * 0.18u'
+ pd='2*int((nf+1)/2) * (W/nf + 0.18u)' ps='2*int((nf+2)/2) * (W/nf + 0.18u)' nrd='0.18u / W' nrs='0.18u / W'
+ sa=0 sb=0 sd=0 m=1
XM29[1] DN D_B AVDD AVDD pfet_03v3 L=0.28u W=0.9u nf=1 ad='int((nf+1)/2) * W/nf * 0.18u' as='int((nf+2)/2) * W/nf * 0.18u'
+ pd='2*int((nf+1)/2) * (W/nf + 0.18u)' ps='2*int((nf+2)/2) * (W/nf + 0.18u)' nrd='0.18u / W' nrs='0.18u / W'
+ sa=0 sb=0 sd=0 m=1
XM29[2] DN D_B AVDD AVDD pfet_03v3 L=0.28u W=0.9u nf=1 ad='int((nf+1)/2) * W/nf * 0.18u' as='int((nf+2)/2) * W/nf * 0.18u'
+ pd='2*int((nf+1)/2) * (W/nf + 0.18u)' ps='2*int((nf+2)/2) * (W/nf + 0.18u)' nrd='0.18u / W' nrs='0.18u / W'
+ sa=0 sb=0 sd=0 m=1
XM29[3] DN D_B AVDD AVDD pfet_03v3 L=0.28u W=0.9u nf=1 ad='int((nf+1)/2) * W/nf * 0.18u' as='int((nf+2)/2) * W/nf * 0.18u'
+ pd='2*int((nf+1)/2) * (W/nf + 0.18u)' ps='2*int((nf+2)/2) * (W/nf + 0.18u)' nrd='0.18u / W' nrs='0.18u / W'
+ sa=0 sb=0 sd=0 m=1
XM29[4] DN D_B AVDD AVDD pfet_03v3 L=0.28u W=0.9u nf=1 ad='int((nf+1)/2) * W/nf * 0.18u' as='int((nf+2)/2) * W/nf * 0.18u'
+ pd='2*int((nf+1)/2) * (W/nf + 0.18u)' ps='2*int((nf+2)/2) * (W/nf + 0.18u)' nrd='0.18u / W' nrs='0.18u / W'
+ sa=0 sb=0 sd=0 m=1
XM29[5] DN D_B AVDD AVDD pfet_03v3 L=0.28u W=0.9u nf=1 ad='int((nf+1)/2) * W/nf * 0.18u' as='int((nf+2)/2) * W/nf * 0.18u'
+ pd='2*int((nf+1)/2) * (W/nf + 0.18u)' ps='2*int((nf+2)/2) * (W/nf + 0.18u)' nrd='0.18u / W' nrs='0.18u / W'
+ sa=0 sb=0 sd=0 m=1
XM29[6] DN D_B AVDD AVDD pfet_03v3 L=0.28u W=0.9u nf=1 ad='int((nf+1)/2) * W/nf * 0.18u' as='int((nf+2)/2) * W/nf * 0.18u'
+ pd='2*int((nf+1)/2) * (W/nf + 0.18u)' ps='2*int((nf+2)/2) * (W/nf + 0.18u)' nrd='0.18u / W' nrs='0.18u / W'
+ sa=0 sb=0 sd=0 m=1
XM29[7] DN D_B AVDD AVDD pfet_03v3 L=0.28u W=0.9u nf=1 ad='int((nf+1)/2) * W/nf * 0.18u' as='int((nf+2)/2) * W/nf * 0.18u'
+ pd='2*int((nf+1)/2) * (W/nf + 0.18u)' ps='2*int((nf+2)/2) * (W/nf + 0.18u)' nrd='0.18u / W' nrs='0.18u / W'
+ sa=0 sb=0 sd=0 m=1
XM30[0] DN D_B GND GND nfet_03v3 L=0.28u W=0.3u nf=1 ad='int((nf+1)/2) * W/nf * 0.18u' as='int((nf+2)/2) * W/nf * 0.18u'
+ pd='2*int((nf+1)/2) * (W/nf + 0.18u)' ps='2*int((nf+2)/2) * (W/nf + 0.18u)' nrd='0.18u / W' nrs='0.18u / W'
+ sa=0 sb=0 sd=0 m=1
XM30[1] DN D_B GND GND nfet_03v3 L=0.28u W=0.3u nf=1 ad='int((nf+1)/2) * W/nf * 0.18u' as='int((nf+2)/2) * W/nf * 0.18u'
+ pd='2*int((nf+1)/2) * (W/nf + 0.18u)' ps='2*int((nf+2)/2) * (W/nf + 0.18u)' nrd='0.18u / W' nrs='0.18u / W'
+ sa=0 sb=0 sd=0 m=1
XM30[2] DN D_B GND GND nfet_03v3 L=0.28u W=0.3u nf=1 ad='int((nf+1)/2) * W/nf * 0.18u' as='int((nf+2)/2) * W/nf * 0.18u'
+ pd='2*int((nf+1)/2) * (W/nf + 0.18u)' ps='2*int((nf+2)/2) * (W/nf + 0.18u)' nrd='0.18u / W' nrs='0.18u / W'
+ sa=0 sb=0 sd=0 m=1
XM30[3] DN D_B GND GND nfet_03v3 L=0.28u W=0.3u nf=1 ad='int((nf+1)/2) * W/nf * 0.18u' as='int((nf+2)/2) * W/nf * 0.18u'
+ pd='2*int((nf+1)/2) * (W/nf + 0.18u)' ps='2*int((nf+2)/2) * (W/nf + 0.18u)' nrd='0.18u / W' nrs='0.18u / W'
+ sa=0 sb=0 sd=0 m=1
XM30[4] DN D_B GND GND nfet_03v3 L=0.28u W=0.3u nf=1 ad='int((nf+1)/2) * W/nf * 0.18u' as='int((nf+2)/2) * W/nf * 0.18u'
+ pd='2*int((nf+1)/2) * (W/nf + 0.18u)' ps='2*int((nf+2)/2) * (W/nf + 0.18u)' nrd='0.18u / W' nrs='0.18u / W'
+ sa=0 sb=0 sd=0 m=1
XM30[5] DN D_B GND GND nfet_03v3 L=0.28u W=0.3u nf=1 ad='int((nf+1)/2) * W/nf * 0.18u' as='int((nf+2)/2) * W/nf * 0.18u'
+ pd='2*int((nf+1)/2) * (W/nf + 0.18u)' ps='2*int((nf+2)/2) * (W/nf + 0.18u)' nrd='0.18u / W' nrs='0.18u / W'
+ sa=0 sb=0 sd=0 m=1
XM30[6] DN D_B GND GND nfet_03v3 L=0.28u W=0.3u nf=1 ad='int((nf+1)/2) * W/nf * 0.18u' as='int((nf+2)/2) * W/nf * 0.18u'
+ pd='2*int((nf+1)/2) * (W/nf + 0.18u)' ps='2*int((nf+2)/2) * (W/nf + 0.18u)' nrd='0.18u / W' nrs='0.18u / W'
+ sa=0 sb=0 sd=0 m=1
XM30[7] DN D_B GND GND nfet_03v3 L=0.28u W=0.3u nf=1 ad='int((nf+1)/2) * W/nf * 0.18u' as='int((nf+2)/2) * W/nf * 0.18u'
+ pd='2*int((nf+1)/2) * (W/nf + 0.18u)' ps='2*int((nf+2)/2) * (W/nf + 0.18u)' nrd='0.18u / W' nrs='0.18u / W'
+ sa=0 sb=0 sd=0 m=1
XM3 D GND D_delay AVDD pfet_03v3 L=0.3u W=1u nf=1 ad='int((nf+1)/2) * W/nf * 0.18u' as='int((nf+2)/2) * W/nf * 0.18u'
+ pd='2*int((nf+1)/2) * (W/nf + 0.18u)' ps='2*int((nf+2)/2) * (W/nf + 0.18u)' nrd='0.18u / W' nrs='0.18u / W'
+ sa=0 sb=0 sd=0 m=1
XM4 D AVDD D_delay GND nfet_03v3 L=0.3u W=0.5u nf=1 ad='int((nf+1)/2) * W/nf * 0.18u' as='int((nf+2)/2) * W/nf * 0.18u'
+ pd='2*int((nf+1)/2) * (W/nf + 0.18u)' ps='2*int((nf+2)/2) * (W/nf + 0.18u)' nrd='0.18u / W' nrs='0.18u / W'
+ sa=0 sb=0 sd=0 m=1
XM1[0] div_outb div_out AVDD AVDD pfet_03v3 L=0.28u W=0.9u nf=1 ad='int((nf+1)/2) * W/nf * 0.18u' as='int((nf+2)/2) * W/nf * 0.18u'
+ pd='2*int((nf+1)/2) * (W/nf + 0.18u)' ps='2*int((nf+2)/2) * (W/nf + 0.18u)' nrd='0.18u / W' nrs='0.18u / W'
+ sa=0 sb=0 sd=0 m=1
XM1[1] div_outb div_out AVDD AVDD pfet_03v3 L=0.28u W=0.9u nf=1 ad='int((nf+1)/2) * W/nf * 0.18u' as='int((nf+2)/2) * W/nf * 0.18u'
+ pd='2*int((nf+1)/2) * (W/nf + 0.18u)' ps='2*int((nf+2)/2) * (W/nf + 0.18u)' nrd='0.18u / W' nrs='0.18u / W'
+ sa=0 sb=0 sd=0 m=1
XM2[0] div_outb div_out GND GND nfet_03v3 L=0.28u W=0.3u nf=1 ad='int((nf+1)/2) * W/nf * 0.18u' as='int((nf+2)/2) * W/nf * 0.18u'
+ pd='2*int((nf+1)/2) * (W/nf + 0.18u)' ps='2*int((nf+2)/2) * (W/nf + 0.18u)' nrd='0.18u / W' nrs='0.18u / W'
+ sa=0 sb=0 sd=0 m=1
XM2[1] div_outb div_out GND GND nfet_03v3 L=0.28u W=0.3u nf=1 ad='int((nf+1)/2) * W/nf * 0.18u' as='int((nf+2)/2) * W/nf * 0.18u'
+ pd='2*int((nf+1)/2) * (W/nf + 0.18u)' ps='2*int((nf+2)/2) * (W/nf + 0.18u)' nrd='0.18u / W' nrs='0.18u / W'
+ sa=0 sb=0 sd=0 m=1
XM3[0] pre_divb pre_div AVDD AVDD pfet_03v3 L=0.28u W=0.9u nf=1 ad='int((nf+1)/2) * W/nf * 0.18u' as='int((nf+2)/2) * W/nf * 0.18u'
+ pd='2*int((nf+1)/2) * (W/nf + 0.18u)' ps='2*int((nf+2)/2) * (W/nf + 0.18u)' nrd='0.18u / W' nrs='0.18u / W'
+ sa=0 sb=0 sd=0 m=1
XM3[1] pre_divb pre_div AVDD AVDD pfet_03v3 L=0.28u W=0.9u nf=1 ad='int((nf+1)/2) * W/nf * 0.18u' as='int((nf+2)/2) * W/nf * 0.18u'
+ pd='2*int((nf+1)/2) * (W/nf + 0.18u)' ps='2*int((nf+2)/2) * (W/nf + 0.18u)' nrd='0.18u / W' nrs='0.18u / W'
+ sa=0 sb=0 sd=0 m=1
XM4[0] pre_divb pre_div GND GND nfet_03v3 L=0.28u W=0.3u nf=1 ad='int((nf+1)/2) * W/nf * 0.18u' as='int((nf+2)/2) * W/nf * 0.18u'
+ pd='2*int((nf+1)/2) * (W/nf + 0.18u)' ps='2*int((nf+2)/2) * (W/nf + 0.18u)' nrd='0.18u / W' nrs='0.18u / W'
+ sa=0 sb=0 sd=0 m=1
XM4[1] pre_divb pre_div GND GND nfet_03v3 L=0.28u W=0.3u nf=1 ad='int((nf+1)/2) * W/nf * 0.18u' as='int((nf+2)/2) * W/nf * 0.18u'
+ pd='2*int((nf+1)/2) * (W/nf + 0.18u)' ps='2*int((nf+2)/2) * (W/nf + 0.18u)' nrd='0.18u / W' nrs='0.18u / W'
+ sa=0 sb=0 sd=0 m=1
**** begin user architecture code


.param f_ref=20MEG R_div=2 N_div=35
*.param f_ref=50e3 R_div=2 N_div=2
.param tp_ref='td_ref/2' td_ref='1/f_ref'
Vref reference gnd pulse(0 3.3 0 10p 10p tp_ref td_ref)

*.ic v(VCTRL)=2.6 v(vbp)=2.6
.ic v(VCTRL)=1.5 v(vbp)=1.5

.ic v(vop1)=3.3 v(von1)=0 v(startup)=0
.options reltol=1e-5 cshunt=1e-15
.options method=gear

*.param d1=0 d2=0 d3=0 d4=0
*.param d1b=3.3 d2b=3.3 d3b=3.3 d4b=3.3

*.param d1=3.3 d2=3.3 d3=3.3 d4=3.3
*.param d1b=0 d2b=0 d3b=0 d4b=0

.param d1=0 d2=3.3 d3=3.3 d4=0
.param d1b=3.3 d2b=0 d3b=0 d4b=3.3

VS1 S1 0 d1
VS2 S2 0 d2
VS3 S3 0 d3
VS4 S4 0 d4

VS1b S1b 0 d1b
VS2b S2b 0 d2b
VS3b S3b 0 d3b
VS4b S4b 0 d4b

.control
set wr_singlescale
set wr_vecnames

* save all
save v(VCTRL) v(vbp) v(vbn) v(reference) v(div_out) v(pre_div) v(div_outb) v(pre_divb) v(phase1)
+ v(phase2) v(phase3) v(phase4) v(up) v(dn)

*v(vop1) v(von1) v(vop3) v(von3)

*OP
*show all

*tran 100n 20m
tran 0.1n 30u 0 5p

remzerovec

*tran 1
*write tb_PLL_CP_VCO_model_R2_N2_350MEG.raw
*tran 2
*write tb_PLL_CP_VCO_PFD_model_R2_N255_255MEG.raw

*tran 3
*write tb_PLL_CP_VCO_PFD_model_R2_N2_50kHz.raw
*tran 4
*write tb_PLL_CP_VCO_model_R2_N255_255kHz.raw
*write tb_PLL_CP_VCO_model_R2_N200_200kHz.raw
wrdata
+ /foss/designs/synchronos-chipathon-2026/designs/libs/scripts/sim_data/tb_PLL_CP_VCO_PFD_model_R2_N35_350MHz.txt tran.all

*tran 5
write tb_PLL_CP_VCO_PFD_model_R2_N35_350MHz.raw

*tran 6

*tran 8

*tran 10

.endc



.include $::180MCU_MODELS/design.ngspice
.lib $::180MCU_MODELS/sm141064.ngspice typical
*.lib $::180MCU_MODELS/sm141064.ngspice SS
*.lib $::180MCU_MODELS/sm141064.ngspice FF
*.lib $::180MCU_MODELS/sm141064.ngspice SF
*.lib $::180MCU_MODELS/sm141064.ngspice FS

**** end user architecture code
**.ends
.end
